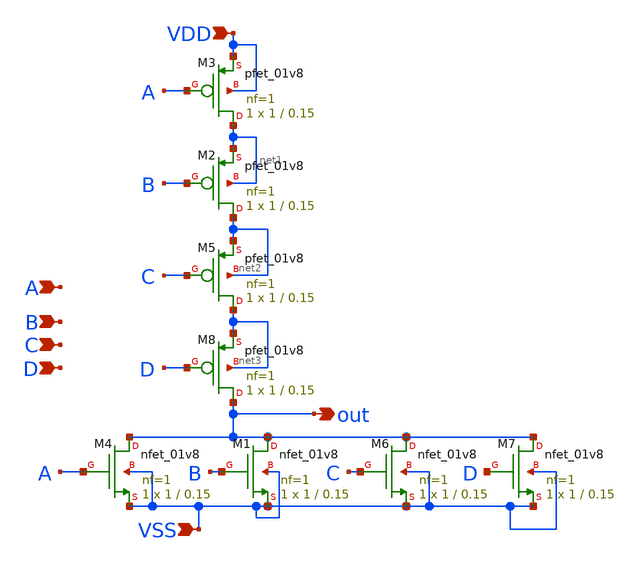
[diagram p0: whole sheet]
** sch_path: nor/nor4.sch
**.subckt nor4 A B out VSS VDD C D
*.ipin A
*.ipin B
*.opin out
*.ipin VSS
*.ipin VDD
*.ipin C
*.ipin D
XM1 out B VSS VSS sky130_fd_pr__nfet_01v8 L=0.15 W=1 nf=1 ad='int((nf+1)/2) * W/nf * 0.29' as='int((nf+2)/2) * W/nf * 0.29'
+ pd='2*int((nf+1)/2) * (W/nf + 0.29)' ps='2*int((nf+2)/2) * (W/nf + 0.29)' nrd='0.29 / W' nrs='0.29 / W'
+ sa=0 sb=0 sd=0 mult=1 m=1
XM2 net2 B net1 net1 sky130_fd_pr__pfet_01v8 L=0.15 W=1 nf=1 ad='int((nf+1)/2) * W/nf * 0.29' as='int((nf+2)/2) * W/nf * 0.29'
+ pd='2*int((nf+1)/2) * (W/nf + 0.29)' ps='2*int((nf+2)/2) * (W/nf + 0.29)' nrd='0.29 / W' nrs='0.29 / W'
+ sa=0 sb=0 sd=0 mult=1 m=1
XM3 net1 A VDD VDD sky130_fd_pr__pfet_01v8 L=0.15 W=1 nf=1 ad='int((nf+1)/2) * W/nf * 0.29' as='int((nf+2)/2) * W/nf * 0.29'
+ pd='2*int((nf+1)/2) * (W/nf + 0.29)' ps='2*int((nf+2)/2) * (W/nf + 0.29)' nrd='0.29 / W' nrs='0.29 / W'
+ sa=0 sb=0 sd=0 mult=1 m=1
XM4 out A VSS VSS sky130_fd_pr__nfet_01v8 L=0.15 W=1 nf=1 ad='int((nf+1)/2) * W/nf * 0.29' as='int((nf+2)/2) * W/nf * 0.29'
+ pd='2*int((nf+1)/2) * (W/nf + 0.29)' ps='2*int((nf+2)/2) * (W/nf + 0.29)' nrd='0.29 / W' nrs='0.29 / W'
+ sa=0 sb=0 sd=0 mult=1 m=1
XM5 net3 C net2 net2 sky130_fd_pr__pfet_01v8 L=0.15 W=1 nf=1 ad='int((nf+1)/2) * W/nf * 0.29' as='int((nf+2)/2) * W/nf * 0.29'
+ pd='2*int((nf+1)/2) * (W/nf + 0.29)' ps='2*int((nf+2)/2) * (W/nf + 0.29)' nrd='0.29 / W' nrs='0.29 / W'
+ sa=0 sb=0 sd=0 mult=1 m=1
XM6 out C VSS VSS sky130_fd_pr__nfet_01v8 L=0.15 W=1 nf=1 ad='int((nf+1)/2) * W/nf * 0.29' as='int((nf+2)/2) * W/nf * 0.29'
+ pd='2*int((nf+1)/2) * (W/nf + 0.29)' ps='2*int((nf+2)/2) * (W/nf + 0.29)' nrd='0.29 / W' nrs='0.29 / W'
+ sa=0 sb=0 sd=0 mult=1 m=1
XM7 out D VSS VSS sky130_fd_pr__nfet_01v8 L=0.15 W=1 nf=1 ad='int((nf+1)/2) * W/nf * 0.29' as='int((nf+2)/2) * W/nf * 0.29'
+ pd='2*int((nf+1)/2) * (W/nf + 0.29)' ps='2*int((nf+2)/2) * (W/nf + 0.29)' nrd='0.29 / W' nrs='0.29 / W'
+ sa=0 sb=0 sd=0 mult=1 m=1
XM8 out D net3 net3 sky130_fd_pr__pfet_01v8 L=0.15 W=1 nf=1 ad='int((nf+1)/2) * W/nf * 0.29' as='int((nf+2)/2) * W/nf * 0.29'
+ pd='2*int((nf+1)/2) * (W/nf + 0.29)' ps='2*int((nf+2)/2) * (W/nf + 0.29)' nrd='0.29 / W' nrs='0.29 / W'
+ sa=0 sb=0 sd=0 mult=1 m=1
**.ends
.end
